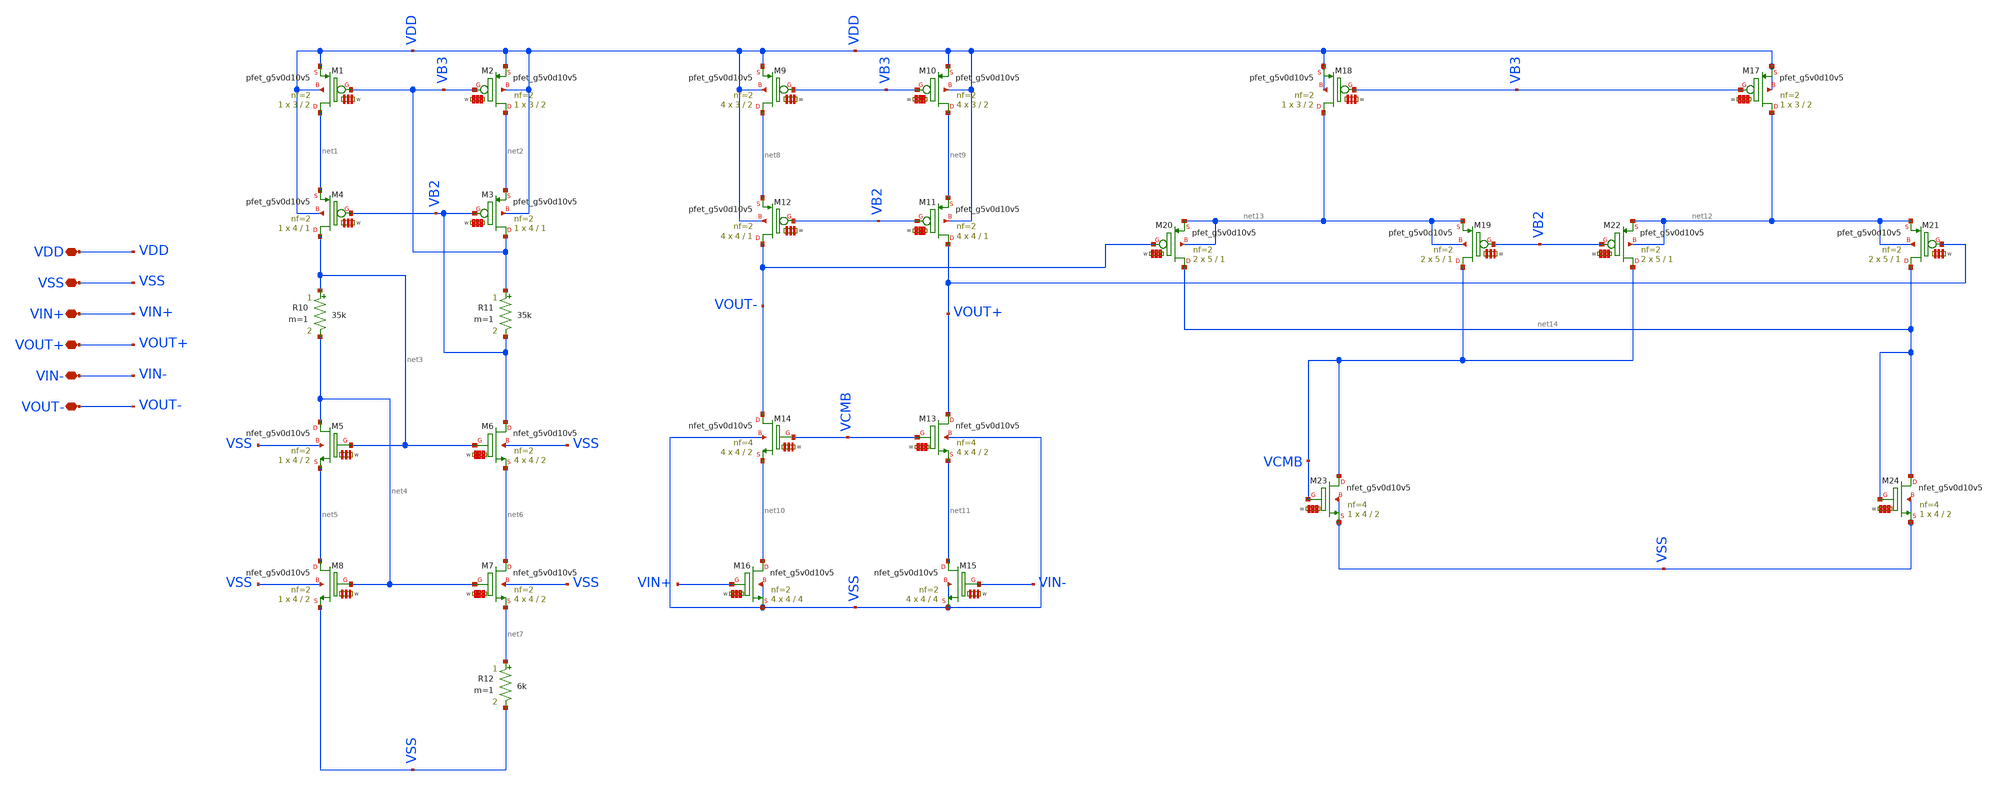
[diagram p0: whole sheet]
** sch_path: my_ip/sky130A/fully_differential_telescopic_cascode_5V_V1/fd_opamp.sch
**.subckt fd_opamp VDD VSS VIN+ VOUT+ VIN- VOUT-
*.iopin VDD
*.iopin VSS
*.iopin VIN+
*.iopin VOUT+
*.iopin VIN-
*.iopin VOUT-
XM1 net1 VB3 VDD VDD sky130_fd_pr__pfet_g5v0d10v5 L=2 W='3 * 2 ' nf=2 ad='int((2 + 1)/2) * 3 * 0.29'
+ as='int((2 + 2)/2) * 3 * 0.29' pd='2*int((2 + 1)/2) * (3 + 0.29)' ps='2*int((2 + 2)/2) * (3 + 0.29)'
+ nrd='0.29 / 3 / 2 ' nrs='0.29 / 3 / 2 ' sa=0 sb=0 sd=0 mult=1 m=1
XM3 VB3 VB2 net2 VDD sky130_fd_pr__pfet_g5v0d10v5 L=1 W='4 * 2 ' nf=2 ad='int((2 + 1)/2) * 4 * 0.29'
+ as='int((2 + 2)/2) * 4 * 0.29' pd='2*int((2 + 1)/2) * (4 + 0.29)' ps='2*int((2 + 2)/2) * (4 + 0.29)'
+ nrd='0.29 / 4 / 2 ' nrs='0.29 / 4 / 2 ' sa=0 sb=0 sd=0 mult=1 m=1
R10 net3 net4 35k m=1
R11 VB3 VB2 35k m=1
XM7 net6 net4 net7 VSS sky130_fd_pr__nfet_g5v0d10v5 L=2 W='4 * 2 ' nf=2 ad='int((nf+1)/2) * W / nf * 0.29'
+ as='int((nf+2)/2) * W / nf * 0.29' pd='2*int((nf+1)/2) * (W / nf + 0.29)' ps='2*int((nf+2)/2) * (W / nf + 0.29)'
+ nrd='0.29 / W ' nrs='0.29 / W ' sa=0 sb=0 sd=0 mult=4 m=4
R12 net7 VSS 6k m=1
XM2 net2 VB3 VDD VDD sky130_fd_pr__pfet_g5v0d10v5 L=2 W='3 * 2 ' nf=2 ad='int((2 + 1)/2) * 3 * 0.29'
+ as='int((2 + 2)/2) * 3 * 0.29' pd='2*int((2 + 1)/2) * (3 + 0.29)' ps='2*int((2 + 2)/2) * (3 + 0.29)'
+ nrd='0.29 / 3 / 2 ' nrs='0.29 / 3 / 2 ' sa=0 sb=0 sd=0 mult=1 m=1
XM6 VB2 net3 net6 VSS sky130_fd_pr__nfet_g5v0d10v5 L=2 W='4 * 2 ' nf=2 ad='int((nf+1)/2) * W / nf * 0.29'
+ as='int((nf+2)/2) * W / nf * 0.29' pd='2*int((nf+1)/2) * (W / nf + 0.29)' ps='2*int((nf+2)/2) * (W / nf + 0.29)'
+ nrd='0.29 / W ' nrs='0.29 / W ' sa=0 sb=0 sd=0 mult=4 m=4
XM5 net4 net3 net5 VSS sky130_fd_pr__nfet_g5v0d10v5 L=2 W='4 * 2 ' nf=2 ad='int((nf+1)/2) * W / nf * 0.29'
+ as='int((nf+2)/2) * W / nf * 0.29' pd='2*int((nf+1)/2) * (W / nf + 0.29)' ps='2*int((nf+2)/2) * (W / nf + 0.29)'
+ nrd='0.29 / W ' nrs='0.29 / W ' sa=0 sb=0 sd=0 mult=1 m=1
XM8 net5 net4 VSS VSS sky130_fd_pr__nfet_g5v0d10v5 L=2 W='4 * 2 ' nf=2 ad='int((nf+1)/2) * W / nf * 0.29'
+ as='int((nf+2)/2) * W / nf * 0.29' pd='2*int((nf+1)/2) * (W / nf + 0.29)' ps='2*int((nf+2)/2) * (W / nf + 0.29)'
+ nrd='0.29 / W ' nrs='0.29 / W ' sa=0 sb=0 sd=0 mult=1 m=1
XM4 net3 VB2 net1 VDD sky130_fd_pr__pfet_g5v0d10v5 L=1 W='4 * 2 ' nf=2 ad='int((2 + 1)/2) * 4 * 0.29'
+ as='int((2 + 2)/2) * 4 * 0.29' pd='2*int((2 + 1)/2) * (4 + 0.29)' ps='2*int((2 + 2)/2) * (4 + 0.29)'
+ nrd='0.29 / 4 / 2 ' nrs='0.29 / 4 / 2 ' sa=0 sb=0 sd=0 mult=1 m=1
XM9 net8 VB3 VDD VDD sky130_fd_pr__pfet_g5v0d10v5 L=2 W='3 * 2 ' nf=2 ad='int((2 + 1)/2) * 3 * 0.29'
+ as='int((2 + 2)/2) * 3 * 0.29' pd='2*int((2 + 1)/2) * (3 + 0.29)' ps='2*int((2 + 2)/2) * (3 + 0.29)'
+ nrd='0.29 / 3 / 2 ' nrs='0.29 / 3 / 2 ' sa=0 sb=0 sd=0 mult=4 m=4
XM10 net9 VB3 VDD VDD sky130_fd_pr__pfet_g5v0d10v5 L=2 W='3 * 2 ' nf=2 ad='int((2 + 1)/2) * 3 * 0.29'
+ as='int((2 + 2)/2) * 3 * 0.29' pd='2*int((2 + 1)/2) * (3 + 0.29)' ps='2*int((2 + 2)/2) * (3 + 0.29)'
+ nrd='0.29 / 3 / 2 ' nrs='0.29 / 3 / 2 ' sa=0 sb=0 sd=0 mult=4 m=4
XM11 VOUT+ VB2 net9 VDD sky130_fd_pr__pfet_g5v0d10v5 L=1 W='4 * 2 ' nf=2 ad='int((2 + 1)/2) * 4 * 0.29'
+ as='int((2 + 2)/2) * 4 * 0.29' pd='2*int((2 + 1)/2) * (4 + 0.29)' ps='2*int((2 + 2)/2) * (4 + 0.29)'
+ nrd='0.29 / 4 / 2 ' nrs='0.29 / 4 / 2 ' sa=0 sb=0 sd=0 mult=4 m=4
XM12 VOUT- VB2 net8 VDD sky130_fd_pr__pfet_g5v0d10v5 L=1 W='4 * 2 ' nf=2 ad='int((2 + 1)/2) * 4 * 0.29'
+ as='int((2 + 2)/2) * 4 * 0.29' pd='2*int((2 + 1)/2) * (4 + 0.29)' ps='2*int((2 + 2)/2) * (4 + 0.29)'
+ nrd='0.29 / 4 / 2 ' nrs='0.29 / 4 / 2 ' sa=0 sb=0 sd=0 mult=4 m=4
XM13 VOUT+ VCMB net11 VSS sky130_fd_pr__nfet_g5v0d10v5 L=2 W='4 * 4 ' nf=4 ad='int((nf+1)/2) * W / nf * 0.29'
+ as='int((nf+2)/2) * W / nf * 0.29' pd='2*int((nf+1)/2) * (W / nf + 0.29)' ps='2*int((nf+2)/2) * (W / nf + 0.29)'
+ nrd='0.29 / W ' nrs='0.29 / W ' sa=0 sb=0 sd=0 mult=4 m=4
XM14 VOUT- VCMB net10 VSS sky130_fd_pr__nfet_g5v0d10v5 L=2 W='4 * 4 ' nf=4 ad='int((nf+1)/2) * W / nf * 0.29'
+ as='int((nf+2)/2) * W / nf * 0.29' pd='2*int((nf+1)/2) * (W / nf + 0.29)' ps='2*int((nf+2)/2) * (W / nf + 0.29)'
+ nrd='0.29 / W ' nrs='0.29 / W ' sa=0 sb=0 sd=0 mult=4 m=4
XM15 net11 VIN- VSS VSS sky130_fd_pr__nfet_g5v0d10v5 L=4 W='4 * 2 ' nf=2 ad='int((nf+1)/2) * W / nf * 0.29'
+ as='int((nf+2)/2) * W / nf * 0.29' pd='2*int((nf+1)/2) * (W / nf + 0.29)' ps='2*int((nf+2)/2) * (W / nf + 0.29)'
+ nrd='0.29 / W ' nrs='0.29 / W ' sa=0 sb=0 sd=0 mult=4 m=4
XM17 net12 VB3 VDD VDD sky130_fd_pr__pfet_g5v0d10v5 L=2 W='3 * 2 ' nf=2 ad='int((2 + 1)/2) * 3 * 0.29'
+ as='int((2 + 2)/2) * 3 * 0.29' pd='2*int((2 + 1)/2) * (3 + 0.29)' ps='2*int((2 + 2)/2) * (3 + 0.29)'
+ nrd='0.29 / 3 / 2 ' nrs='0.29 / 3 / 2 ' sa=0 sb=0 sd=0 mult=1 m=1
XM18 net13 VB3 VDD VDD sky130_fd_pr__pfet_g5v0d10v5 L=2 W='3 * 2 ' nf=2 ad='int((2 + 1)/2) * 3 * 0.29'
+ as='int((2 + 2)/2) * 3 * 0.29' pd='2*int((2 + 1)/2) * (3 + 0.29)' ps='2*int((2 + 2)/2) * (3 + 0.29)'
+ nrd='0.29 / 3 / 2 ' nrs='0.29 / 3 / 2 ' sa=0 sb=0 sd=0 mult=1 m=1
XM23 VCMB VCMB VSS VSS sky130_fd_pr__nfet_g5v0d10v5 L=2 W='4 * 4 ' nf=4 ad='int((nf+1)/2) * W / nf * 0.29'
+ as='int((nf+2)/2) * W / nf * 0.29' pd='2*int((nf+1)/2) * (W / nf + 0.29)' ps='2*int((nf+2)/2) * (W / nf + 0.29)'
+ nrd='0.29 / W ' nrs='0.29 / W ' sa=0 sb=0 sd=0 mult=1 m=1
XM19 VCMB VB2 net13 net13 sky130_fd_pr__pfet_g5v0d10v5 L=1 W='5 * 2 ' nf=2 ad='int((2 + 1)/2) * 5 * 0.29'
+ as='int((2 + 2)/2) * 5 * 0.29' pd='2*int((2 + 1)/2) * (5 + 0.29)' ps='2*int((2 + 2)/2) * (5 + 0.29)'
+ nrd='0.29 / 5 / 2 ' nrs='0.29 / 5 / 2 ' sa=0 sb=0 sd=0 mult=2 m=2
XM20 net14 VOUT- net13 net13 sky130_fd_pr__pfet_g5v0d10v5 L=1 W='5 * 2 ' nf=2 ad='int((2 + 1)/2) * 5 * 0.29'
+ as='int((2 + 2)/2) * 5 * 0.29' pd='2*int((2 + 1)/2) * (5 + 0.29)' ps='2*int((2 + 2)/2) * (5 + 0.29)'
+ nrd='0.29 / 5 / 2 ' nrs='0.29 / 5 / 2 ' sa=0 sb=0 sd=0 mult=2 m=2
XM21 net14 VOUT+ net12 net12 sky130_fd_pr__pfet_g5v0d10v5 L=1 W='5 * 2 ' nf=2 ad='int((2 + 1)/2) * 5 * 0.29'
+ as='int((2 + 2)/2) * 5 * 0.29' pd='2*int((2 + 1)/2) * (5 + 0.29)' ps='2*int((2 + 2)/2) * (5 + 0.29)'
+ nrd='0.29 / 5 / 2 ' nrs='0.29 / 5 / 2 ' sa=0 sb=0 sd=0 mult=2 m=2
XM22 VCMB VB2 net12 net12 sky130_fd_pr__pfet_g5v0d10v5 L=1 W='5 * 2 ' nf=2 ad='int((2 + 1)/2) * 5 * 0.29'
+ as='int((2 + 2)/2) * 5 * 0.29' pd='2*int((2 + 1)/2) * (5 + 0.29)' ps='2*int((2 + 2)/2) * (5 + 0.29)'
+ nrd='0.29 / 5 / 2 ' nrs='0.29 / 5 / 2 ' sa=0 sb=0 sd=0 mult=2 m=2
XM24 net14 net14 VSS VSS sky130_fd_pr__nfet_g5v0d10v5 L=2 W='4 * 4 ' nf=4 ad='int((nf+1)/2) * W / nf * 0.29'
+ as='int((nf+2)/2) * W / nf * 0.29' pd='2*int((nf+1)/2) * (W / nf + 0.29)' ps='2*int((nf+2)/2) * (W / nf + 0.29)'
+ nrd='0.29 / W ' nrs='0.29 / W ' sa=0 sb=0 sd=0 mult=1 m=1
XM16 net10 VIN+ VSS VSS sky130_fd_pr__nfet_g5v0d10v5 L=4 W='4 * 2 ' nf=2 ad='int((nf+1)/2) * W / nf * 0.29'
+ as='int((nf+2)/2) * W / nf * 0.29' pd='2*int((nf+1)/2) * (W / nf + 0.29)' ps='2*int((nf+2)/2) * (W / nf + 0.29)'
+ nrd='0.29 / W ' nrs='0.29 / W ' sa=0 sb=0 sd=0 mult=4 m=4
**.ends
.end
